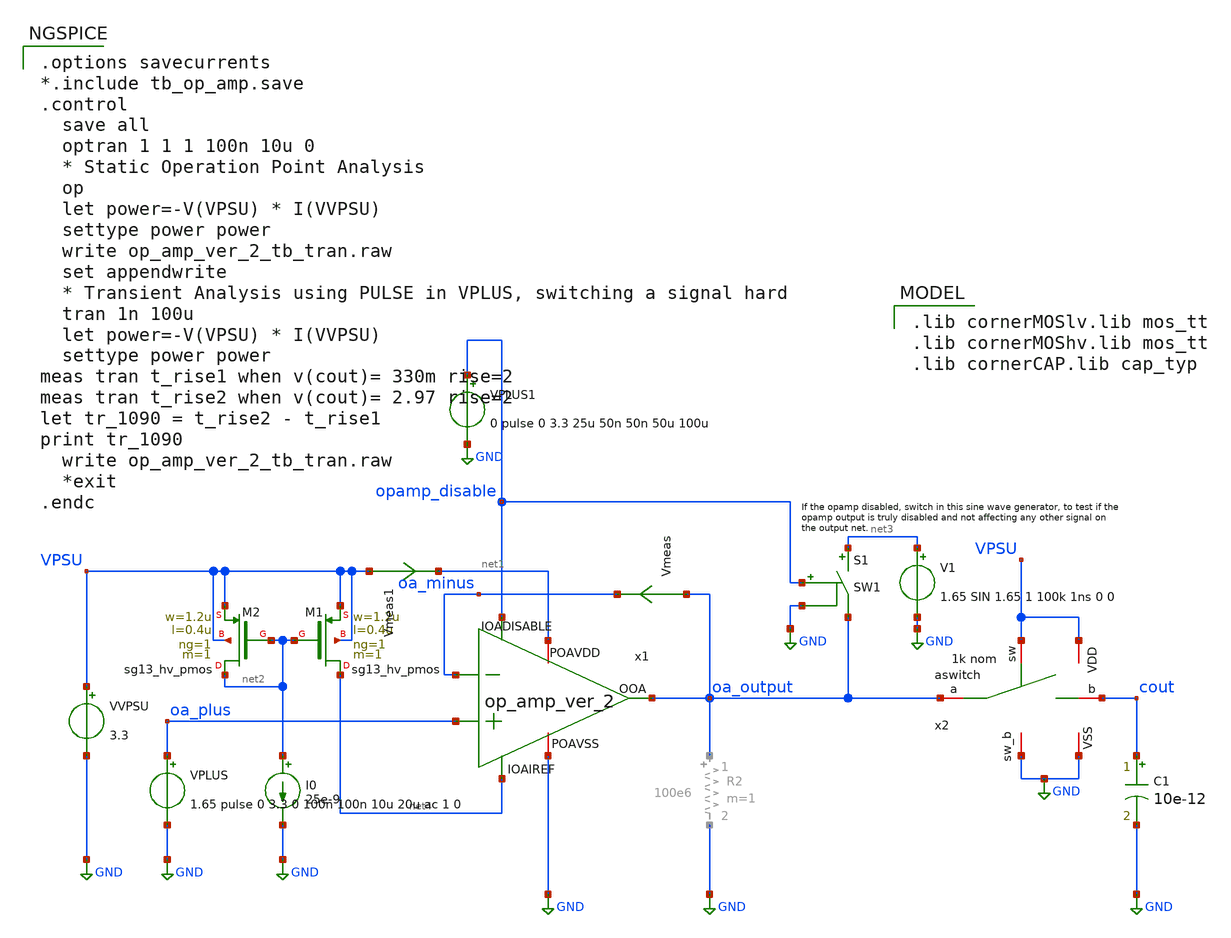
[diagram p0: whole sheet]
** sch_path: macros/heichips26_FAIf/macros/opamp/testbenches/xschem/opa_ver2_Csamp_slew_tb_tran.sch
**.subckt opa_ver2_Csamp_slew_tb_tran
VVPSU VPSU GND 3.3
I0 net2 GND 25e-9
VPLUS oa_plus GND 1.65 pulse 0 3.3 0 100n 100n 10u 20u ac 1 0
C1 cout GND 10e-12 m=1
Vmeas oa_output oa_minus 0
.save i(vmeas)
VPLUS1 opamp_disable GND 0 pulse 0 3.3 25u 50n 50n 50u 100u
XM1 net4 net2 VPSU VPSU sg13_hv_pmos w=1.2u l=0.4u ng=1 m=1 mm_ok=1
XM2 net2 net2 VPSU VPSU sg13_hv_pmos w=1.2u l=0.4u ng=1 m=1 mm_ok=1
V1 net3 GND 1.65 SIN 1.65 1 100k 1ns 0 0
S1 net3 oa_output opamp_disable GND SW1
Vmeas1 VPSU net1 0
.save i(vmeas1)
x1 net1 net4 oa_minus oa_output oa_plus GND opamp_disable op_amp_ver_2
x2 GND VPSU cout oa_output GND VPSU aswitch
**** begin user architecture code

.lib cornerMOSlv.lib mos_tt
.lib cornerMOShv.lib mos_tt
.lib cornerCAP.lib cap_typ



.options savecurrents
*.include tb_op_amp.save
.control
  save all
  optran 1 1 1 100n 10u 0
  * Static Operation Point Analysis
  op
  let power=-V(VPSU) * I(VVPSU)
  settype power power
  write op_amp_ver_2_tb_tran.raw
  set appendwrite
  * Transient Analysis using PULSE in VPLUS, switching a signal hard
  tran 1n 100u
  let power=-V(VPSU) * I(VVPSU)
  settype power power
meas tran t_rise1 when v(cout)= 330m rise=2
meas tran t_rise2 when v(cout)= 2.97 rise=2
let tr_1090 = t_rise2 - t_rise1
print tr_1090
  write op_amp_ver_2_tb_tran.raw
  *exit
.endc


**** end user architecture code
**.ends
.GLOBAL GND
**** begin user architecture code
.MODEL SW1 SW   VT=3 VH=0.01  RON=1k ROFF=10G
**** end user architecture code
.end
